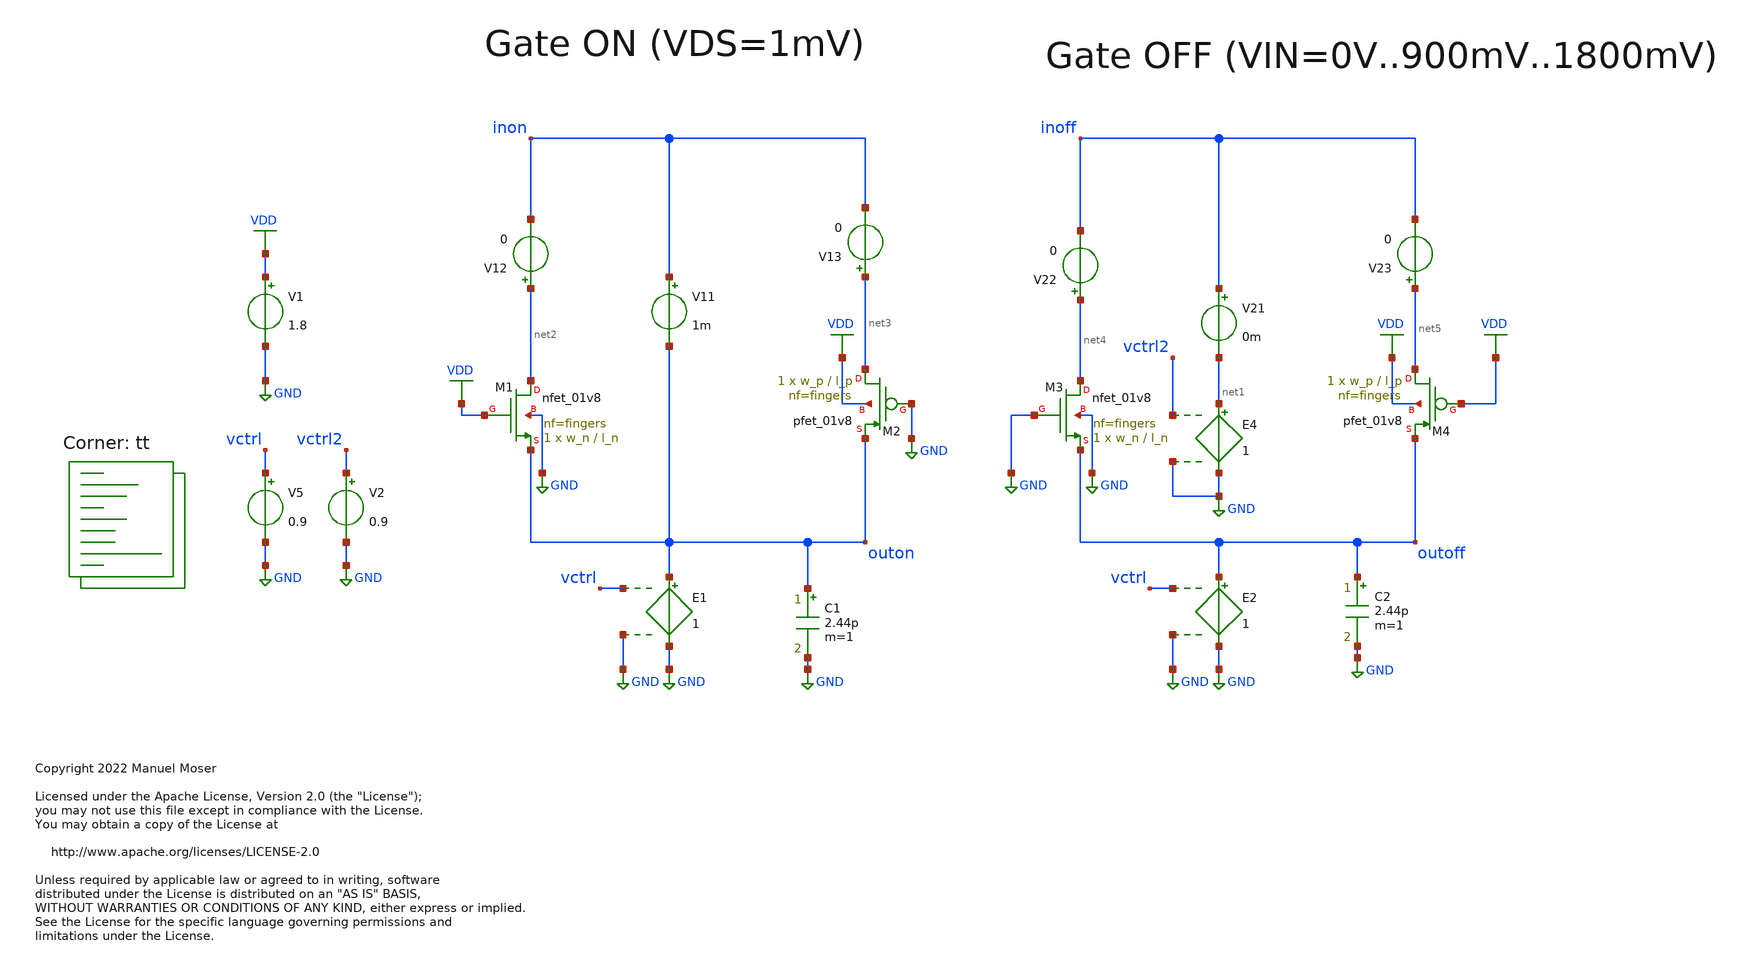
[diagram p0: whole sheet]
** sch_path: xschem/adc_gate_tb_resistance_01v8.sch
* Copyright 2022 Manuel Moser
* Licensed under the Apache License, Version 2.0 (the "License");
**.subckt adc_gate_tb_resistance_01v8
V5 vctrl GND 0.9
XM1 net2 VDD outon GND sky130_fd_pr__nfet_01v8 L=l_n W=w_n nf=fingers ad='int((nf+1)/2) * W/nf * 0.29'
+ as='int((nf+2)/2) * W/nf * 0.29' pd='2*int((nf+1)/2) * (W/nf + 0.29)' ps='2*int((nf+2)/2) * (W/nf + 0.29)'
+ nrd='0.29 / W' nrs='0.29 / W' sa=0 sb=0 sd=0 mult=1 m=1
XM2 net3 GND outon VDD sky130_fd_pr__pfet_01v8 L=l_p W=w_p nf=fingers ad='int((nf+1)/2) * W/nf * 0.29'
+ as='int((nf+2)/2) * W/nf * 0.29' pd='2*int((nf+1)/2) * (W/nf + 0.29)' ps='2*int((nf+2)/2) * (W/nf + 0.29)'
+ nrd='0.29 / W' nrs='0.29 / W' sa=0 sb=0 sd=0 mult=1 m=1
XM3 net4 GND outoff GND sky130_fd_pr__nfet_01v8 L=l_n W=w_n nf=fingers ad='int((nf+1)/2) * W/nf * 0.29'
+ as='int((nf+2)/2) * W/nf * 0.29' pd='2*int((nf+1)/2) * (W/nf + 0.29)' ps='2*int((nf+2)/2) * (W/nf + 0.29)'
+ nrd='0.29 / W' nrs='0.29 / W' sa=0 sb=0 sd=0 mult=1 m=1
XM4 net5 VDD outoff VDD sky130_fd_pr__pfet_01v8 L=l_p W=w_p nf=fingers ad='int((nf+1)/2) * W/nf * 0.29'
+ as='int((nf+2)/2) * W/nf * 0.29' pd='2*int((nf+1)/2) * (W/nf + 0.29)' ps='2*int((nf+2)/2) * (W/nf + 0.29)'
+ nrd='0.29 / W' nrs='0.29 / W' sa=0 sb=0 sd=0 mult=1 m=1
E1 outon GND vctrl GND 1
E2 outoff GND vctrl GND 1
C1 outon GND 2.44p m=1
C2 outoff GND 2.44p m=1
E4 net1 GND vctrl2 GND 1
V21 inoff net1 0m
V11 inon outon 1m
V12 net2 inon 0
V13 net3 inon 0
V22 net4 inoff 0
V23 net5 inoff 0
V1 VDD GND 1.8
V2 vctrl2 GND 0.9
**** begin user architecture code
.lib $::SKYWATER_MODELS/sky130.lib.spice tt


.save all
.temp =25
*.options method=gear
.OPTIONS savecurrents
*.OPTIONS RELTOL=.1 TRTOL=1 ABSTOL=1e-20 CHGTOL=1.0e-20 DEFAD=1.0e-18
.save @m.x1.xm1.msky130_fd_pr__pfet_01v8[gm]
.save @m.x1.xm1.msky130_fd_pr__pfet_01v8[CGS]
.save @m.x1.xm1.msky130_fd_pr__pfet_01v8[Vth]
.save @m.x1.xm2.msky130_fd_pr__nfet_01v8_lvt[gm]
.save @m.x1.xm2.msky130_fd_pr__nfet_01v8_lvt[CGS]
.save @m.x1.xm2.msky130_fd_pr__nfet_01v8_lvt[Vth]

.param w_p=1
.param l_p = 1
.param w_n=1
.param l_n=1
.param fingers=1
.param VIN = 1.8

.dc V5 100m 1.7 10m V2 0 1.8 900m

.control
alterparam w_p=0.42
alterparam l_p=0.15
alterparam w_n=0.42
alterparam l_n=0.15

reset
run
write dc-sweep.out I(v11) I(v12) I(v13) I(v21) I(v22) I(v23) v(inon) v(outon) v(inoff) v(outoff)
set appendwrite

*********************************************************

alterparam w_p=0.42
alterparam l_p=0.24
alterparam w_n=0.42
alterparam l_n=0.24

reset
run
write dc-sweep.out I(v11) I(v12) I(v13) I(v21) I(v22) I(v23) v(inon) v(outon) v(inoff) v(outoff)
set appendwrite


*********************************************************

alterparam w_p=16
alterparam l_p=0.24
alterparam w_n=16
alterparam l_n=0.24
alterparam fingers=8

reset
run
write dc-sweep.out I(v11) I(v12) I(v13) I(v21) I(v22) I(v23) v(inon) v(outon) v(inoff) v(outoff)
set appendwrite

*********************************************************

*On-Resistance
plot (-(dc1.v(inon)-dc1.v(outon))/dc1.I(v11)) (-(dc2.v(inon)-dc2.v(outon))/dc2.I(v11)) (-(dc3.v(inon)-dc3.v(outon))/dc3.I(v11))
+ ylog xlabel 'Vout' ylabel 'on-resistance in ohm' title 'RON with VDS=1mV'

*Off-Leakage
plot (-dc1.I(v21)) (-dc2.I(v21)) (-dc3.I(v21)) ylimit -50p 50p xlabel 'output voltage' ylabel 'Leakage current in A'
+ title 'leakage currents with VDS=0V..900mV..1.8V'

.endc


**** end user architecture code
**.ends
.GLOBAL GND
.GLOBAL VDD
.end
